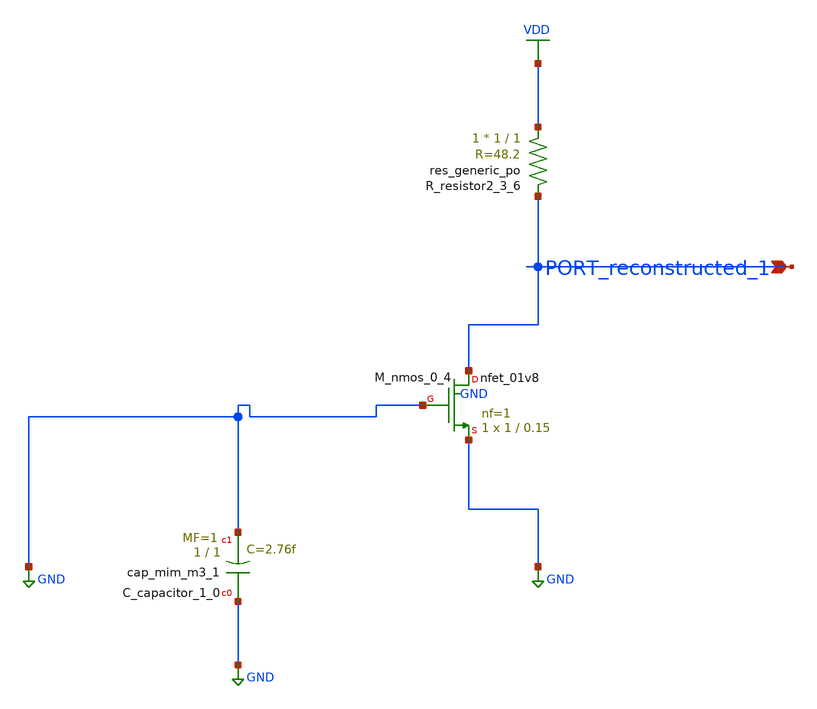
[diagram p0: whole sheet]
** sch_path: schematics/AMSNet/500.sch
**.subckt 500 PORT_reconstructed_1
*.ipin PORT_reconstructed_1
XC_capacitor_1_0 GND GND sky130_fd_pr__cap_mim_m3_1 W=1 L=1 MF=1 m=1
XM_nmos_0_4 PORT_reconstructed_1 GND GND GND sky130_fd_pr__nfet_01v8 L=0.15 W=1 nf=1 ad='int((1 + 1)/2) * 1 / 1 * 0.29'
+ as='int((1 + 2)/2) * 1 / 1 * 0.29' pd='2*int((1 + 1)/2) * (1 / 1 + 0.29)' ps='2*int((1 + 2)/2) * (1 / 1 + 0.29)'
+ nrd='0.29 / 1 ' nrs='0.29 / 1 ' sa=0 sb=0 sd=0 mult=1 m=1
XR_resistor2_3_6 VDD PORT_reconstructed_1 sky130_fd_pr__res_generic_po W=1 L=1 m=1
**.ends
.GLOBAL GND
.GLOBAL VDD
.end
